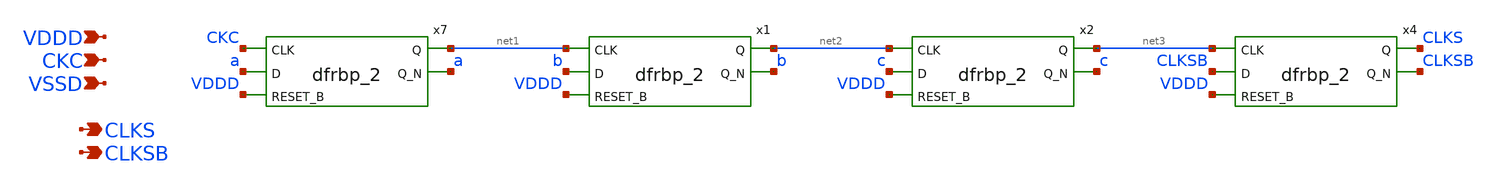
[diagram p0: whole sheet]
** sch_path: xschem/auto_sampling.sch
**.subckt auto_sampling CKC VDDD VSSD CLKS CLKSB
*.ipin CKC
*.ipin VDDD
*.ipin VSSD
*.opin CLKS
*.opin CLKSB
x7 CKC a VDDD VSSD VSSD VDDD VDDD net1 a sky130_fd_sc_hd__dfrbp_2
x1 net1 b VDDD VSSD VSSD VDDD VDDD net2 b sky130_fd_sc_hd__dfrbp_2
x2 net2 c VDDD VSSD VSSD VDDD VDDD net3 c sky130_fd_sc_hd__dfrbp_2
x4 net3 CLKSB VDDD VSSD VSSD VDDD VDDD CLKS CLKSB sky130_fd_sc_hd__dfrbp_2
**.ends
.end
